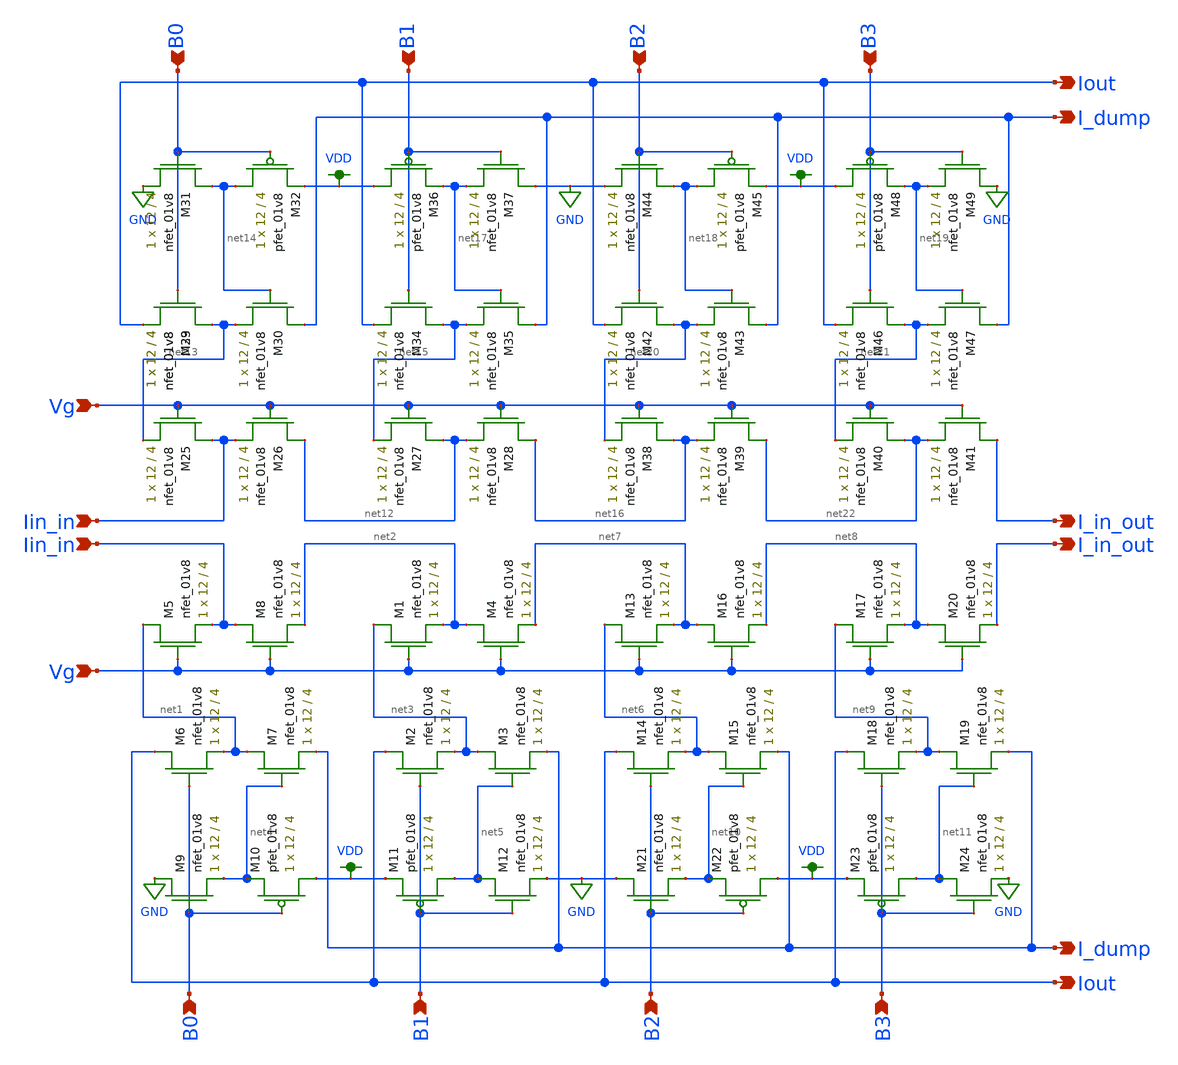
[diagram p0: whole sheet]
** sch_path: modules/ladder_lds.sch
**.subckt ladder_lds Iin_in Vg B0 I_dump Iout B1 B2 B3 Iin_in Vg B0 B1 B2 B3 I_dump Iout I_in_out
*+ I_in_out
*.ipin Iin_in
*.ipin Vg
*.ipin B0
*.opin I_dump
*.opin Iout
*.ipin B1
*.ipin B2
*.ipin B3
*.ipin Iin_in
*.ipin Vg
*.ipin B0
*.ipin B1
*.ipin B2
*.ipin B3
*.opin I_dump
*.opin Iout
*.opin I_in_out
*.opin I_in_out
XM5 net1 Vg Iin_in GND sky130_fd_pr__nfet_01v8 L=4 W=12 nf=1 ad='int((nf+1)/2) * W/nf * 0.29' as='int((nf+2)/2) * W/nf * 0.29'
+ pd='2*int((nf+1)/2) * (W/nf + 0.29)' ps='2*int((nf+2)/2) * (W/nf + 0.29)' nrd='0.29 / W' nrs='0.29 / W'
+ sa=0 sb=0 sd=0 mult=1 m=1
XM6 Iout B0 net1 GND sky130_fd_pr__nfet_01v8 L=4 W=12 nf=1 ad='int((nf+1)/2) * W/nf * 0.29' as='int((nf+2)/2) * W/nf * 0.29'
+ pd='2*int((nf+1)/2) * (W/nf + 0.29)' ps='2*int((nf+2)/2) * (W/nf + 0.29)' nrd='0.29 / W' nrs='0.29 / W'
+ sa=0 sb=0 sd=0 mult=1 m=1
XM7 net1 net4 I_dump GND sky130_fd_pr__nfet_01v8 L=4 W=12 nf=1 ad='int((nf+1)/2) * W/nf * 0.29' as='int((nf+2)/2) * W/nf * 0.29'
+ pd='2*int((nf+1)/2) * (W/nf + 0.29)' ps='2*int((nf+2)/2) * (W/nf + 0.29)' nrd='0.29 / W' nrs='0.29 / W'
+ sa=0 sb=0 sd=0 mult=1 m=1
XM8 Iin_in Vg net2 GND sky130_fd_pr__nfet_01v8 L=4 W=12 nf=1 ad='int((nf+1)/2) * W/nf * 0.29' as='int((nf+2)/2) * W/nf * 0.29'
+ pd='2*int((nf+1)/2) * (W/nf + 0.29)' ps='2*int((nf+2)/2) * (W/nf + 0.29)' nrd='0.29 / W' nrs='0.29 / W'
+ sa=0 sb=0 sd=0 mult=1 m=1
XM1 net3 Vg net2 GND sky130_fd_pr__nfet_01v8 L=4 W=12 nf=1 ad='int((nf+1)/2) * W/nf * 0.29' as='int((nf+2)/2) * W/nf * 0.29'
+ pd='2*int((nf+1)/2) * (W/nf + 0.29)' ps='2*int((nf+2)/2) * (W/nf + 0.29)' nrd='0.29 / W' nrs='0.29 / W'
+ sa=0 sb=0 sd=0 mult=1 m=1
XM2 Iout B1 net3 GND sky130_fd_pr__nfet_01v8 L=4 W=12 nf=1 ad='int((nf+1)/2) * W/nf * 0.29' as='int((nf+2)/2) * W/nf * 0.29'
+ pd='2*int((nf+1)/2) * (W/nf + 0.29)' ps='2*int((nf+2)/2) * (W/nf + 0.29)' nrd='0.29 / W' nrs='0.29 / W'
+ sa=0 sb=0 sd=0 mult=1 m=1
XM3 net3 net5 I_dump GND sky130_fd_pr__nfet_01v8 L=4 W=12 nf=1 ad='int((nf+1)/2) * W/nf * 0.29' as='int((nf+2)/2) * W/nf * 0.29'
+ pd='2*int((nf+1)/2) * (W/nf + 0.29)' ps='2*int((nf+2)/2) * (W/nf + 0.29)' nrd='0.29 / W' nrs='0.29 / W'
+ sa=0 sb=0 sd=0 mult=1 m=1
XM4 net2 Vg net7 GND sky130_fd_pr__nfet_01v8 L=4 W=12 nf=1 ad='int((nf+1)/2) * W/nf * 0.29' as='int((nf+2)/2) * W/nf * 0.29'
+ pd='2*int((nf+1)/2) * (W/nf + 0.29)' ps='2*int((nf+2)/2) * (W/nf + 0.29)' nrd='0.29 / W' nrs='0.29 / W'
+ sa=0 sb=0 sd=0 mult=1 m=1
XM9 GND B0 net4 GND sky130_fd_pr__nfet_01v8 L=4 W=12 nf=1 ad='int((nf+1)/2) * W/nf * 0.29' as='int((nf+2)/2) * W/nf * 0.29'
+ pd='2*int((nf+1)/2) * (W/nf + 0.29)' ps='2*int((nf+2)/2) * (W/nf + 0.29)' nrd='0.29 / W' nrs='0.29 / W'
+ sa=0 sb=0 sd=0 mult=1 m=1
XM10 VDD B0 net4 VDD sky130_fd_pr__pfet_01v8 L=4 W=12 nf=1 ad='int((nf+1)/2) * W/nf * 0.29' as='int((nf+2)/2) * W/nf * 0.29'
+ pd='2*int((nf+1)/2) * (W/nf + 0.29)' ps='2*int((nf+2)/2) * (W/nf + 0.29)' nrd='0.29 / W' nrs='0.29 / W'
+ sa=0 sb=0 sd=0 mult=1 m=1
XM12 net5 B1 GND GND sky130_fd_pr__nfet_01v8 L=4 W=12 nf=1 ad='int((nf+1)/2) * W/nf * 0.29' as='int((nf+2)/2) * W/nf * 0.29'
+ pd='2*int((nf+1)/2) * (W/nf + 0.29)' ps='2*int((nf+2)/2) * (W/nf + 0.29)' nrd='0.29 / W' nrs='0.29 / W'
+ sa=0 sb=0 sd=0 mult=1 m=1
XM13 net6 Vg net7 GND sky130_fd_pr__nfet_01v8 L=4 W=12 nf=1 ad='int((nf+1)/2) * W/nf * 0.29' as='int((nf+2)/2) * W/nf * 0.29'
+ pd='2*int((nf+1)/2) * (W/nf + 0.29)' ps='2*int((nf+2)/2) * (W/nf + 0.29)' nrd='0.29 / W' nrs='0.29 / W'
+ sa=0 sb=0 sd=0 mult=1 m=1
XM14 Iout B2 net6 GND sky130_fd_pr__nfet_01v8 L=4 W=12 nf=1 ad='int((nf+1)/2) * W/nf * 0.29' as='int((nf+2)/2) * W/nf * 0.29'
+ pd='2*int((nf+1)/2) * (W/nf + 0.29)' ps='2*int((nf+2)/2) * (W/nf + 0.29)' nrd='0.29 / W' nrs='0.29 / W'
+ sa=0 sb=0 sd=0 mult=1 m=1
XM15 net6 net10 I_dump GND sky130_fd_pr__nfet_01v8 L=4 W=12 nf=1 ad='int((nf+1)/2) * W/nf * 0.29' as='int((nf+2)/2) * W/nf * 0.29'
+ pd='2*int((nf+1)/2) * (W/nf + 0.29)' ps='2*int((nf+2)/2) * (W/nf + 0.29)' nrd='0.29 / W' nrs='0.29 / W'
+ sa=0 sb=0 sd=0 mult=1 m=1
XM16 net7 Vg net8 GND sky130_fd_pr__nfet_01v8 L=4 W=12 nf=1 ad='int((nf+1)/2) * W/nf * 0.29' as='int((nf+2)/2) * W/nf * 0.29'
+ pd='2*int((nf+1)/2) * (W/nf + 0.29)' ps='2*int((nf+2)/2) * (W/nf + 0.29)' nrd='0.29 / W' nrs='0.29 / W'
+ sa=0 sb=0 sd=0 mult=1 m=1
XM17 net9 Vg net8 GND sky130_fd_pr__nfet_01v8 L=4 W=12 nf=1 ad='int((nf+1)/2) * W/nf * 0.29' as='int((nf+2)/2) * W/nf * 0.29'
+ pd='2*int((nf+1)/2) * (W/nf + 0.29)' ps='2*int((nf+2)/2) * (W/nf + 0.29)' nrd='0.29 / W' nrs='0.29 / W'
+ sa=0 sb=0 sd=0 mult=1 m=1
XM18 Iout B3 net9 GND sky130_fd_pr__nfet_01v8 L=4 W=12 nf=1 ad='int((nf+1)/2) * W/nf * 0.29' as='int((nf+2)/2) * W/nf * 0.29'
+ pd='2*int((nf+1)/2) * (W/nf + 0.29)' ps='2*int((nf+2)/2) * (W/nf + 0.29)' nrd='0.29 / W' nrs='0.29 / W'
+ sa=0 sb=0 sd=0 mult=1 m=1
XM19 net9 net11 I_dump GND sky130_fd_pr__nfet_01v8 L=4 W=12 nf=1 ad='int((nf+1)/2) * W/nf * 0.29' as='int((nf+2)/2) * W/nf * 0.29'
+ pd='2*int((nf+1)/2) * (W/nf + 0.29)' ps='2*int((nf+2)/2) * (W/nf + 0.29)' nrd='0.29 / W' nrs='0.29 / W'
+ sa=0 sb=0 sd=0 mult=1 m=1
XM20 net8 Vg I_in_out GND sky130_fd_pr__nfet_01v8 L=4 W=12 nf=1 ad='int((nf+1)/2) * W/nf * 0.29' as='int((nf+2)/2) * W/nf * 0.29'
+ pd='2*int((nf+1)/2) * (W/nf + 0.29)' ps='2*int((nf+2)/2) * (W/nf + 0.29)' nrd='0.29 / W' nrs='0.29 / W'
+ sa=0 sb=0 sd=0 mult=1 m=1
XM21 GND B2 net10 GND sky130_fd_pr__nfet_01v8 L=4 W=12 nf=1 ad='int((nf+1)/2) * W/nf * 0.29' as='int((nf+2)/2) * W/nf * 0.29'
+ pd='2*int((nf+1)/2) * (W/nf + 0.29)' ps='2*int((nf+2)/2) * (W/nf + 0.29)' nrd='0.29 / W' nrs='0.29 / W'
+ sa=0 sb=0 sd=0 mult=1 m=1
XM24 net11 B3 GND GND sky130_fd_pr__nfet_01v8 L=4 W=12 nf=1 ad='int((nf+1)/2) * W/nf * 0.29' as='int((nf+2)/2) * W/nf * 0.29'
+ pd='2*int((nf+1)/2) * (W/nf + 0.29)' ps='2*int((nf+2)/2) * (W/nf + 0.29)' nrd='0.29 / W' nrs='0.29 / W'
+ sa=0 sb=0 sd=0 mult=1 m=1
XM11 net5 B1 VDD VDD sky130_fd_pr__pfet_01v8 L=4 W=12 nf=1 ad='int((nf+1)/2) * W/nf * 0.29' as='int((nf+2)/2) * W/nf * 0.29'
+ pd='2*int((nf+1)/2) * (W/nf + 0.29)' ps='2*int((nf+2)/2) * (W/nf + 0.29)' nrd='0.29 / W' nrs='0.29 / W'
+ sa=0 sb=0 sd=0 mult=1 m=1
XM22 VDD B2 net10 VDD sky130_fd_pr__pfet_01v8 L=4 W=12 nf=1 ad='int((nf+1)/2) * W/nf * 0.29' as='int((nf+2)/2) * W/nf * 0.29'
+ pd='2*int((nf+1)/2) * (W/nf + 0.29)' ps='2*int((nf+2)/2) * (W/nf + 0.29)' nrd='0.29 / W' nrs='0.29 / W'
+ sa=0 sb=0 sd=0 mult=1 m=1
XM23 net11 B3 VDD VDD sky130_fd_pr__pfet_01v8 L=4 W=12 nf=1 ad='int((nf+1)/2) * W/nf * 0.29' as='int((nf+2)/2) * W/nf * 0.29'
+ pd='2*int((nf+1)/2) * (W/nf + 0.29)' ps='2*int((nf+2)/2) * (W/nf + 0.29)' nrd='0.29 / W' nrs='0.29 / W'
+ sa=0 sb=0 sd=0 mult=1 m=1
XM25 Iin_in Vg net13 GND sky130_fd_pr__nfet_01v8 L=4 W=12 nf=1 ad='int((nf+1)/2) * W/nf * 0.29' as='int((nf+2)/2) * W/nf * 0.29'
+ pd='2*int((nf+1)/2) * (W/nf + 0.29)' ps='2*int((nf+2)/2) * (W/nf + 0.29)' nrd='0.29 / W' nrs='0.29 / W'
+ sa=0 sb=0 sd=0 mult=1 m=1
XM26 net12 Vg Iin_in GND sky130_fd_pr__nfet_01v8 L=4 W=12 nf=1 ad='int((nf+1)/2) * W/nf * 0.29' as='int((nf+2)/2) * W/nf * 0.29'
+ pd='2*int((nf+1)/2) * (W/nf + 0.29)' ps='2*int((nf+2)/2) * (W/nf + 0.29)' nrd='0.29 / W' nrs='0.29 / W'
+ sa=0 sb=0 sd=0 mult=1 m=1
XM27 net12 Vg net15 GND sky130_fd_pr__nfet_01v8 L=4 W=12 nf=1 ad='int((nf+1)/2) * W/nf * 0.29' as='int((nf+2)/2) * W/nf * 0.29'
+ pd='2*int((nf+1)/2) * (W/nf + 0.29)' ps='2*int((nf+2)/2) * (W/nf + 0.29)' nrd='0.29 / W' nrs='0.29 / W'
+ sa=0 sb=0 sd=0 mult=1 m=1
XM28 net16 Vg net12 GND sky130_fd_pr__nfet_01v8 L=4 W=12 nf=1 ad='int((nf+1)/2) * W/nf * 0.29' as='int((nf+2)/2) * W/nf * 0.29'
+ pd='2*int((nf+1)/2) * (W/nf + 0.29)' ps='2*int((nf+2)/2) * (W/nf + 0.29)' nrd='0.29 / W' nrs='0.29 / W'
+ sa=0 sb=0 sd=0 mult=1 m=1
XM29 net13 B0 Iout GND sky130_fd_pr__nfet_01v8 L=4 W=12 nf=1 ad='int((nf+1)/2) * W/nf * 0.29' as='int((nf+2)/2) * W/nf * 0.29'
+ pd='2*int((nf+1)/2) * (W/nf + 0.29)' ps='2*int((nf+2)/2) * (W/nf + 0.29)' nrd='0.29 / W' nrs='0.29 / W'
+ sa=0 sb=0 sd=0 mult=1 m=1
XM30 I_dump net14 net13 GND sky130_fd_pr__nfet_01v8 L=4 W=12 nf=1 ad='int((nf+1)/2) * W/nf * 0.29' as='int((nf+2)/2) * W/nf * 0.29'
+ pd='2*int((nf+1)/2) * (W/nf + 0.29)' ps='2*int((nf+2)/2) * (W/nf + 0.29)' nrd='0.29 / W' nrs='0.29 / W'
+ sa=0 sb=0 sd=0 mult=1 m=1
XM31 net14 B0 GND GND sky130_fd_pr__nfet_01v8 L=4 W=12 nf=1 ad='int((nf+1)/2) * W/nf * 0.29' as='int((nf+2)/2) * W/nf * 0.29'
+ pd='2*int((nf+1)/2) * (W/nf + 0.29)' ps='2*int((nf+2)/2) * (W/nf + 0.29)' nrd='0.29 / W' nrs='0.29 / W'
+ sa=0 sb=0 sd=0 mult=1 m=1
XM32 net14 B0 VDD VDD sky130_fd_pr__pfet_01v8 L=4 W=12 nf=1 ad='int((nf+1)/2) * W/nf * 0.29' as='int((nf+2)/2) * W/nf * 0.29'
+ pd='2*int((nf+1)/2) * (W/nf + 0.29)' ps='2*int((nf+2)/2) * (W/nf + 0.29)' nrd='0.29 / W' nrs='0.29 / W'
+ sa=0 sb=0 sd=0 mult=1 m=1
XM33 net13 B0 Iout GND sky130_fd_pr__nfet_01v8 L=4 W=12 nf=1 ad='int((nf+1)/2) * W/nf * 0.29' as='int((nf+2)/2) * W/nf * 0.29'
+ pd='2*int((nf+1)/2) * (W/nf + 0.29)' ps='2*int((nf+2)/2) * (W/nf + 0.29)' nrd='0.29 / W' nrs='0.29 / W'
+ sa=0 sb=0 sd=0 mult=1 m=1
XM34 net15 B1 Iout GND sky130_fd_pr__nfet_01v8 L=4 W=12 nf=1 ad='int((nf+1)/2) * W/nf * 0.29' as='int((nf+2)/2) * W/nf * 0.29'
+ pd='2*int((nf+1)/2) * (W/nf + 0.29)' ps='2*int((nf+2)/2) * (W/nf + 0.29)' nrd='0.29 / W' nrs='0.29 / W'
+ sa=0 sb=0 sd=0 mult=1 m=1
XM35 I_dump net17 net15 GND sky130_fd_pr__nfet_01v8 L=4 W=12 nf=1 ad='int((nf+1)/2) * W/nf * 0.29' as='int((nf+2)/2) * W/nf * 0.29'
+ pd='2*int((nf+1)/2) * (W/nf + 0.29)' ps='2*int((nf+2)/2) * (W/nf + 0.29)' nrd='0.29 / W' nrs='0.29 / W'
+ sa=0 sb=0 sd=0 mult=1 m=1
XM36 VDD B1 net17 VDD sky130_fd_pr__pfet_01v8 L=4 W=12 nf=1 ad='int((nf+1)/2) * W/nf * 0.29' as='int((nf+2)/2) * W/nf * 0.29'
+ pd='2*int((nf+1)/2) * (W/nf + 0.29)' ps='2*int((nf+2)/2) * (W/nf + 0.29)' nrd='0.29 / W' nrs='0.29 / W'
+ sa=0 sb=0 sd=0 mult=1 m=1
XM37 GND B1 net17 GND sky130_fd_pr__nfet_01v8 L=4 W=12 nf=1 ad='int((nf+1)/2) * W/nf * 0.29' as='int((nf+2)/2) * W/nf * 0.29'
+ pd='2*int((nf+1)/2) * (W/nf + 0.29)' ps='2*int((nf+2)/2) * (W/nf + 0.29)' nrd='0.29 / W' nrs='0.29 / W'
+ sa=0 sb=0 sd=0 mult=1 m=1
XM38 net16 Vg net20 GND sky130_fd_pr__nfet_01v8 L=4 W=12 nf=1 ad='int((nf+1)/2) * W/nf * 0.29' as='int((nf+2)/2) * W/nf * 0.29'
+ pd='2*int((nf+1)/2) * (W/nf + 0.29)' ps='2*int((nf+2)/2) * (W/nf + 0.29)' nrd='0.29 / W' nrs='0.29 / W'
+ sa=0 sb=0 sd=0 mult=1 m=1
XM39 net22 Vg net16 GND sky130_fd_pr__nfet_01v8 L=4 W=12 nf=1 ad='int((nf+1)/2) * W/nf * 0.29' as='int((nf+2)/2) * W/nf * 0.29'
+ pd='2*int((nf+1)/2) * (W/nf + 0.29)' ps='2*int((nf+2)/2) * (W/nf + 0.29)' nrd='0.29 / W' nrs='0.29 / W'
+ sa=0 sb=0 sd=0 mult=1 m=1
XM40 net22 Vg net21 GND sky130_fd_pr__nfet_01v8 L=4 W=12 nf=1 ad='int((nf+1)/2) * W/nf * 0.29' as='int((nf+2)/2) * W/nf * 0.29'
+ pd='2*int((nf+1)/2) * (W/nf + 0.29)' ps='2*int((nf+2)/2) * (W/nf + 0.29)' nrd='0.29 / W' nrs='0.29 / W'
+ sa=0 sb=0 sd=0 mult=1 m=1
XM41 I_in_out Vg net22 GND sky130_fd_pr__nfet_01v8 L=4 W=12 nf=1 ad='int((nf+1)/2) * W/nf * 0.29' as='int((nf+2)/2) * W/nf * 0.29'
+ pd='2*int((nf+1)/2) * (W/nf + 0.29)' ps='2*int((nf+2)/2) * (W/nf + 0.29)' nrd='0.29 / W' nrs='0.29 / W'
+ sa=0 sb=0 sd=0 mult=1 m=1
XM42 net20 B2 Iout GND sky130_fd_pr__nfet_01v8 L=4 W=12 nf=1 ad='int((nf+1)/2) * W/nf * 0.29' as='int((nf+2)/2) * W/nf * 0.29'
+ pd='2*int((nf+1)/2) * (W/nf + 0.29)' ps='2*int((nf+2)/2) * (W/nf + 0.29)' nrd='0.29 / W' nrs='0.29 / W'
+ sa=0 sb=0 sd=0 mult=1 m=1
XM43 I_dump net18 net20 GND sky130_fd_pr__nfet_01v8 L=4 W=12 nf=1 ad='int((nf+1)/2) * W/nf * 0.29' as='int((nf+2)/2) * W/nf * 0.29'
+ pd='2*int((nf+1)/2) * (W/nf + 0.29)' ps='2*int((nf+2)/2) * (W/nf + 0.29)' nrd='0.29 / W' nrs='0.29 / W'
+ sa=0 sb=0 sd=0 mult=1 m=1
XM44 net18 B2 GND GND sky130_fd_pr__nfet_01v8 L=4 W=12 nf=1 ad='int((nf+1)/2) * W/nf * 0.29' as='int((nf+2)/2) * W/nf * 0.29'
+ pd='2*int((nf+1)/2) * (W/nf + 0.29)' ps='2*int((nf+2)/2) * (W/nf + 0.29)' nrd='0.29 / W' nrs='0.29 / W'
+ sa=0 sb=0 sd=0 mult=1 m=1
XM45 net18 B2 VDD VDD sky130_fd_pr__pfet_01v8 L=4 W=12 nf=1 ad='int((nf+1)/2) * W/nf * 0.29' as='int((nf+2)/2) * W/nf * 0.29'
+ pd='2*int((nf+1)/2) * (W/nf + 0.29)' ps='2*int((nf+2)/2) * (W/nf + 0.29)' nrd='0.29 / W' nrs='0.29 / W'
+ sa=0 sb=0 sd=0 mult=1 m=1
XM46 net21 B3 Iout GND sky130_fd_pr__nfet_01v8 L=4 W=12 nf=1 ad='int((nf+1)/2) * W/nf * 0.29' as='int((nf+2)/2) * W/nf * 0.29'
+ pd='2*int((nf+1)/2) * (W/nf + 0.29)' ps='2*int((nf+2)/2) * (W/nf + 0.29)' nrd='0.29 / W' nrs='0.29 / W'
+ sa=0 sb=0 sd=0 mult=1 m=1
XM47 I_dump net19 net21 GND sky130_fd_pr__nfet_01v8 L=4 W=12 nf=1 ad='int((nf+1)/2) * W/nf * 0.29' as='int((nf+2)/2) * W/nf * 0.29'
+ pd='2*int((nf+1)/2) * (W/nf + 0.29)' ps='2*int((nf+2)/2) * (W/nf + 0.29)' nrd='0.29 / W' nrs='0.29 / W'
+ sa=0 sb=0 sd=0 mult=1 m=1
XM48 VDD B3 net19 VDD sky130_fd_pr__pfet_01v8 L=4 W=12 nf=1 ad='int((nf+1)/2) * W/nf * 0.29' as='int((nf+2)/2) * W/nf * 0.29'
+ pd='2*int((nf+1)/2) * (W/nf + 0.29)' ps='2*int((nf+2)/2) * (W/nf + 0.29)' nrd='0.29 / W' nrs='0.29 / W'
+ sa=0 sb=0 sd=0 mult=1 m=1
XM49 GND B3 net19 GND sky130_fd_pr__nfet_01v8 L=4 W=12 nf=1 ad='int((nf+1)/2) * W/nf * 0.29' as='int((nf+2)/2) * W/nf * 0.29'
+ pd='2*int((nf+1)/2) * (W/nf + 0.29)' ps='2*int((nf+2)/2) * (W/nf + 0.29)' nrd='0.29 / W' nrs='0.29 / W'
+ sa=0 sb=0 sd=0 mult=1 m=1
**.ends
.GLOBAL GND
.GLOBAL VDD
.end
